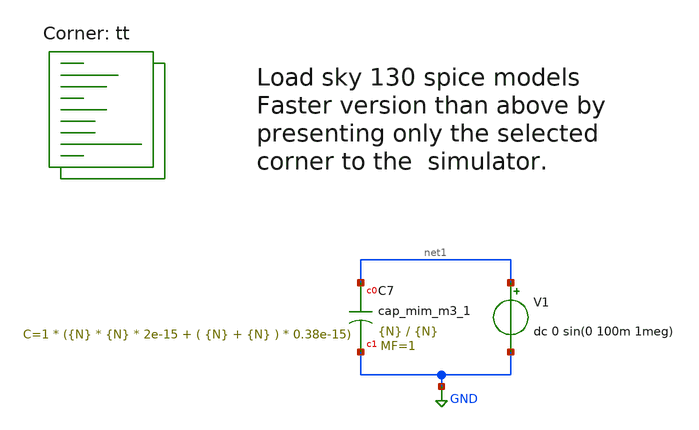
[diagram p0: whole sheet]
** sch_path: CTLE/passive_mimcap_sweep.sch
**.subckt passive_mimcap_sweep
XC7 net1 GND sky130_fd_pr__cap_mim_m3_1 W={N} L={N} MF=1 m=1
V1 net1 GND dc 0 sin(0 100m 1meg)
.save i(v1)
**** begin user architecture code



  .param corner_factor=0
  .param process_mc_factor=0
  .param mc_pr_switch=0
  .param mc_mm_switch=0
  .param mismatch_factor=0
  .param sw_mm_cmim=0

  .tran 10n 10u
  .control
    let freq = 1e6
    let omega = 2 * 3.14159265 * freq
    let idx = 0
    let Cvec = unitvec(91)
    foreach N 1 1.1 1.2 1.3 1.4 1.5 1.6 1.7 1.8 1.9 2 2.1 2.2 2.3 2.4 2.5 2.6 2.7 2.8 2.9 3 3.1 3.2
+ 3.3 3.4 3.5 3.6 3.7 3.8 3.9 4 4.1 4.2 4.3 4.4 4.5 4.6 4.7 4.8 4.9 5 5.1 5.2 5.3 5.4 5.5 5.6 5.7 5.8 5.9
+ 6 6.1 6.2 6.3 6.4 6.5 6.6 6.7 6.8 6.9 7 7.1 7.2 7.3 7.4 7.5 7.6 7.7 7.8 7.9 8 8.1 8.2 8.3 8.4 8.5 8.6
+ 8.7 8.8 8.9 9 9.1 9.2 9.3 9.4 9.5 9.6 9.7 9.8 9.9 10
      alterparam N = $N
      reset
      run
      let Imag = rms(i(V1))
      let Cscalar = Imag / omega
      let Cvec[idx] = mean(Cscalar)
      let idx = idx + 1
    end
    plot Cvec title 'MIM Cap: C vs N (W=L=N, MF=1)'
  .endc



.lib $::SKYWATER_MODELS/sky130.lib.spice tt
**** end user architecture code
**.ends
.GLOBAL GND
.end
